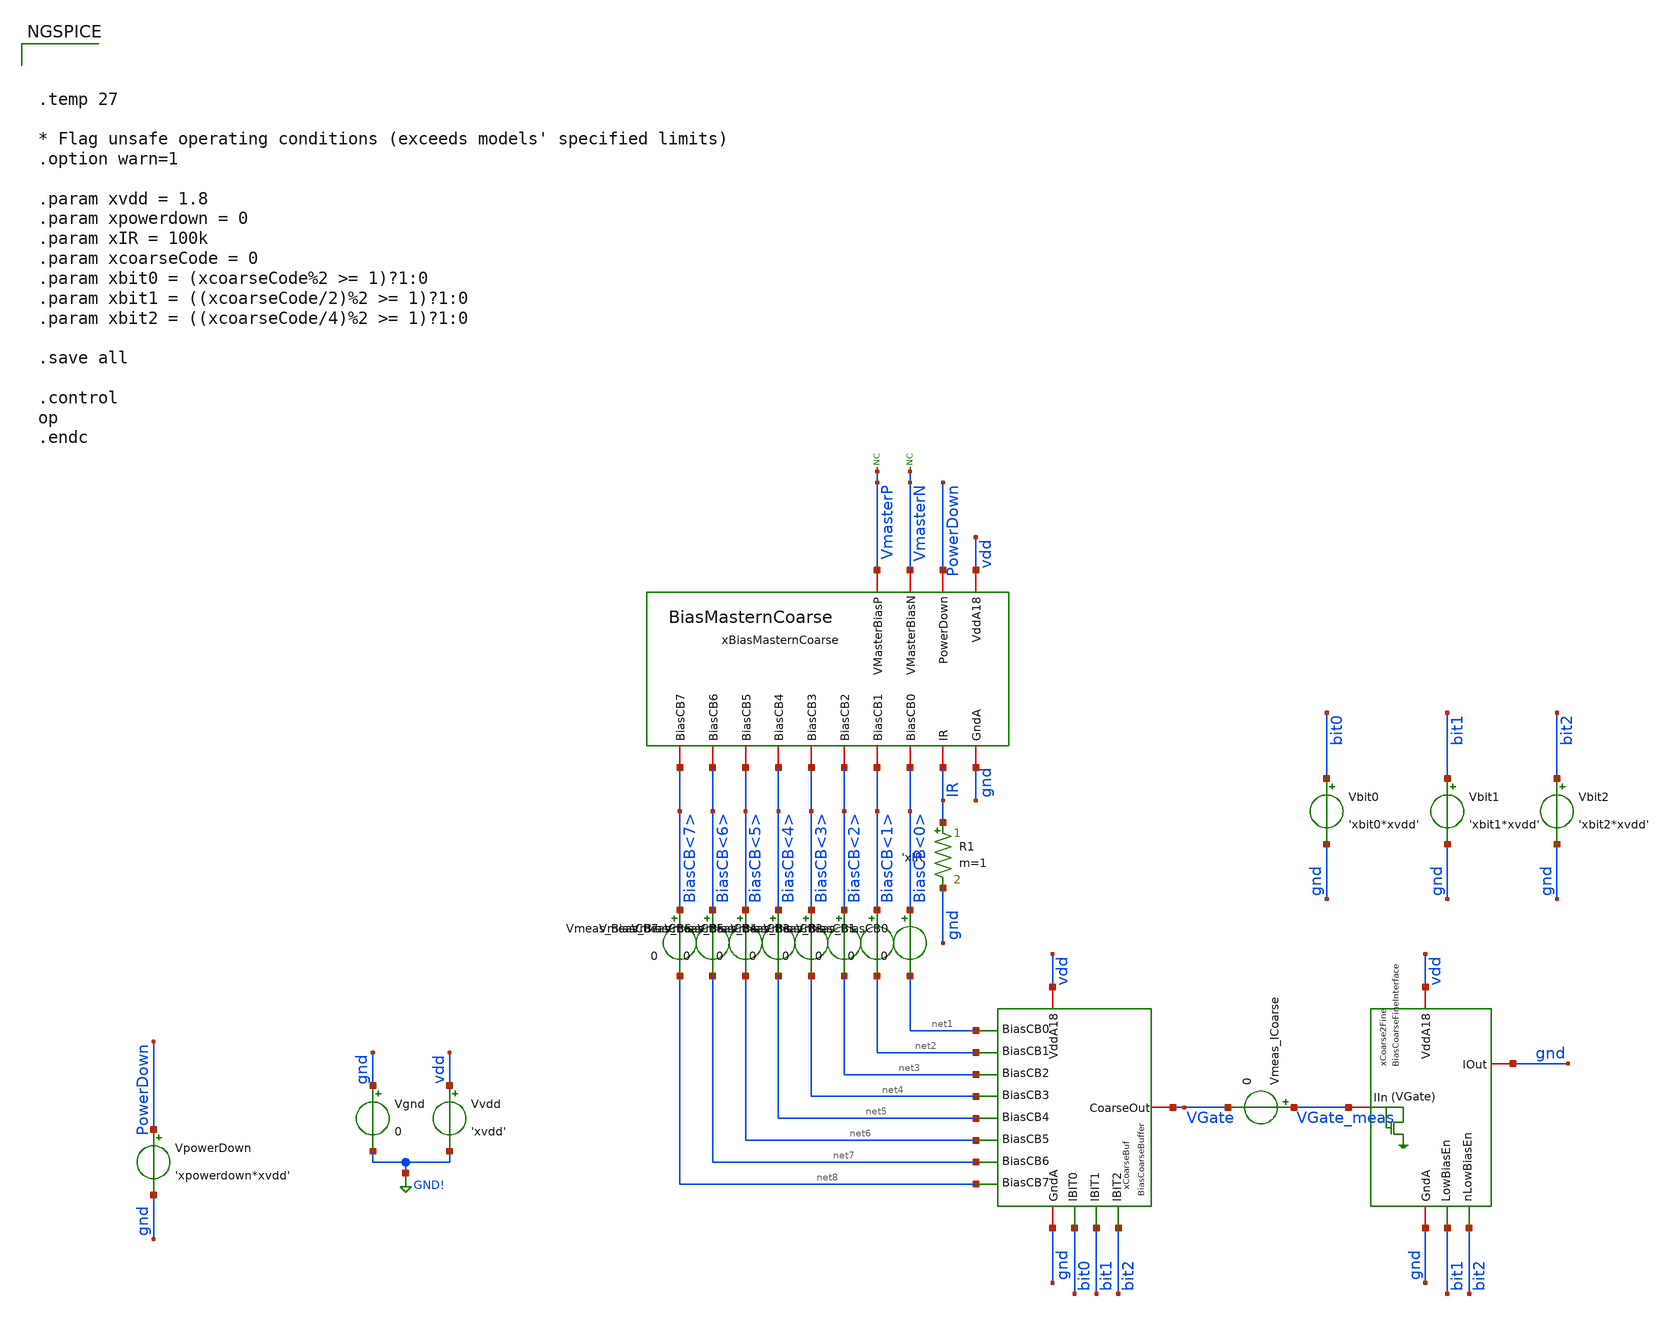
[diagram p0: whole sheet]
** sch_path: analog/xschem/tb_BiasCoarseBuffer.sch
**.subckt tb_BiasCoarseBuffer
Vgnd gnd GND! 0
.save i(vgnd)
Vvdd vdd GND! 'xvdd'
.save i(vvdd)
R1 IR gnd 'xIR' m=1
VpowerDown PowerDown gnd 'xpowerdown*xvdd'
.save i(vpowerdown)
* noconn VmasterN
* noconn VmasterP
xCoarseBuf vdd gnd bit0 bit1 bit2 VGate net1 net2 net4 net5 net6 net7 net8 net3 BiasCoarseBuffer
xBiasMasternCoarse vdd gnd BiasCB<0> BiasCB<1> BiasCB<3> BiasCB<4> BiasCB<5> BiasCB<6> BiasCB<7>
+ BiasCB<2> PowerDown VmasterN VmasterP IR BiasMasternCoarse
Vmeas_BiasCB0 BiasCB<0> net1 0
.save i(vmeas_biascb0)
Vmeas_BiasCB1 BiasCB<1> net2 0
.save i(vmeas_biascb1)
Vmeas_BiasCB2 BiasCB<2> net3 0
.save i(vmeas_biascb2)
Vmeas_BiasCB3 BiasCB<3> net4 0
.save i(vmeas_biascb3)
Vmeas_BiasCB4 BiasCB<4> net5 0
.save i(vmeas_biascb4)
Vmeas_BiasCB5 BiasCB<5> net6 0
.save i(vmeas_biascb5)
Vmeas_BiasCB6 BiasCB<6> net7 0
.save i(vmeas_biascb6)
Vmeas_BiasCB7 BiasCB<7> net8 0
.save i(vmeas_biascb7)
xCoarse2Fine vdd gnd bit1 bit2 VGate_meas gnd BiasCoarseFineInterface
Vmeas_ICoarse VGate_meas VGate 0
.save i(vmeas_icoarse)
Vbit0 bit0 gnd 'xbit0*xvdd'
.save i(vbit0)
Vbit1 bit1 gnd 'xbit1*xvdd'
.save i(vbit1)
Vbit2 bit2 gnd 'xbit2*xvdd'
.save i(vbit2)
**** begin user architecture code

** opencircuitdesign pdks install
.lib $::SKYWATER_MODELS/sky130.lib.spice tt




.temp 27

* Flag unsafe operating conditions (exceeds models' specified limits)
.option warn=1

.param xvdd = 1.8
.param xpowerdown = 0
.param xIR = 100k
.param xcoarseCode = 0
.param xbit0 = (xcoarseCode%2 >= 1)?1:0
.param xbit1 = ((xcoarseCode/2)%2 >= 1)?1:0
.param xbit2 = ((xcoarseCode/4)%2 >= 1)?1:0

.save all

.control
op
.endc


**** end user architecture code
**.ends
.GLOBAL GND!
.end
